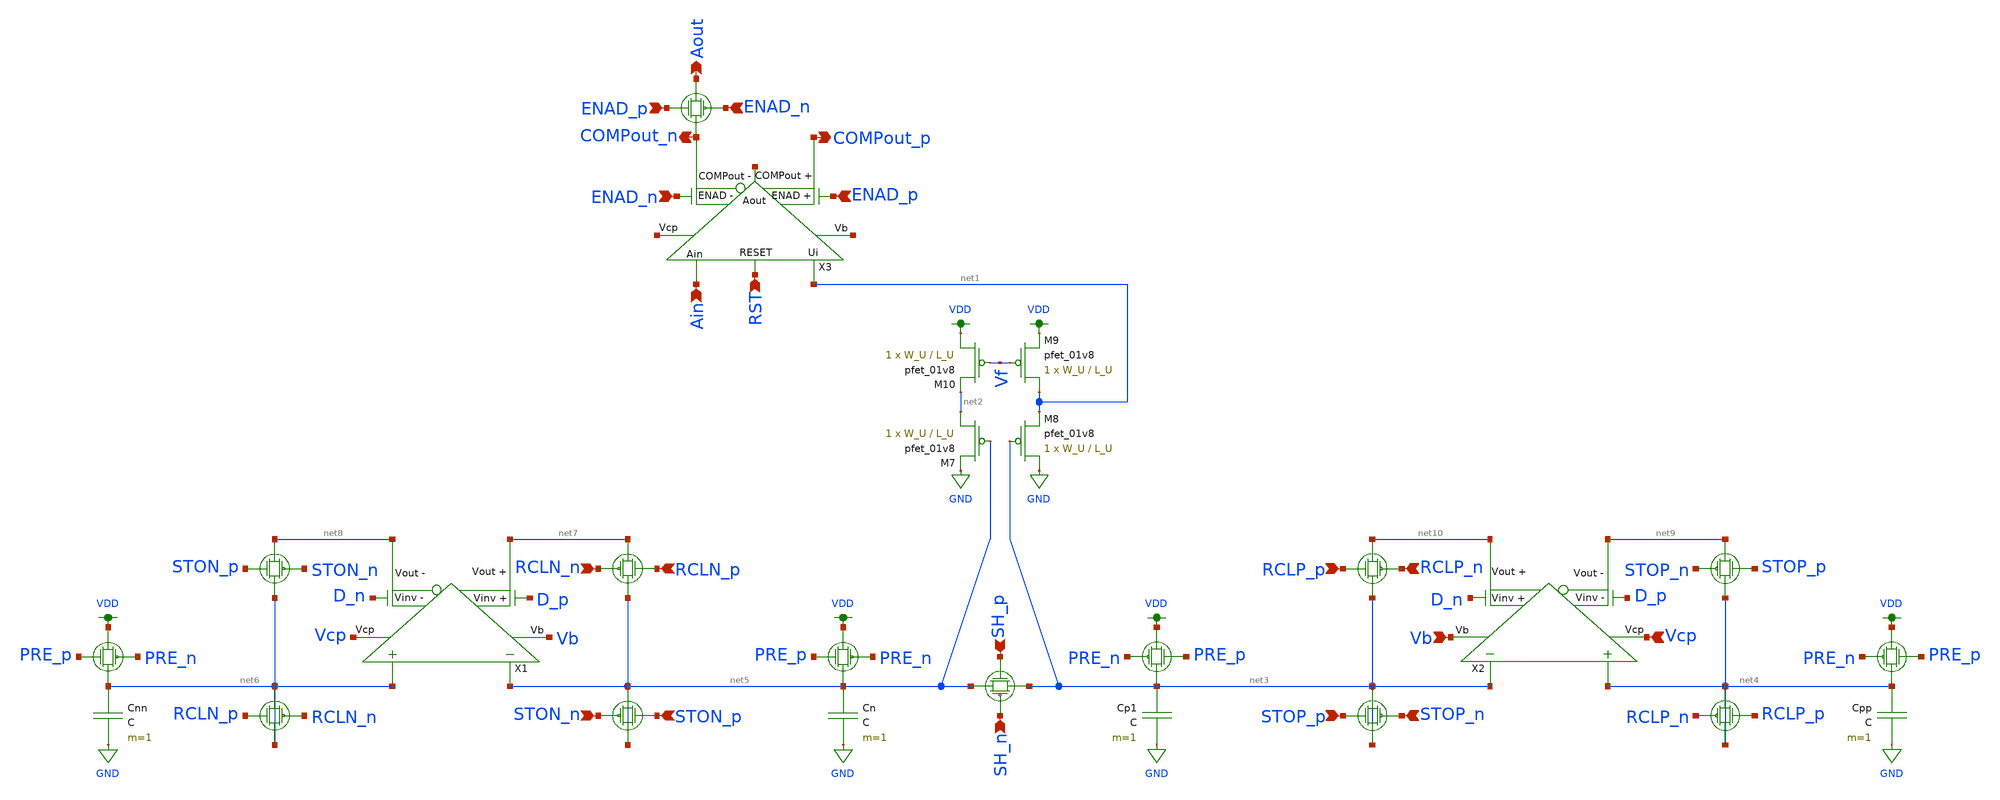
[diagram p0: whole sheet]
** sch_path: schematics/toplevel_pretty.sch
**.subckt toplevel_pretty RCLP_p STOP_p RCLP_n STOP_n SH_p SH_n Vb Vcp RCLN_p STON_p RCLN_n STON_n
*+ RST Ain Aout COMPout_n COMPout_p ENAD_p ENAD_n ENAD_p ENAD_n
*.ipin RCLP_p
*.ipin STOP_p
*.ipin RCLP_n
*.ipin STOP_n
*.ipin SH_p
*.ipin SH_n
*.ipin Vb
*.ipin Vcp
*.ipin RCLN_p
*.ipin STON_p
*.ipin RCLN_n
*.ipin STON_n
*.ipin RST
*.ipin Ain
*.opin Aout
*.opin COMPout_n
*.opin COMPout_p
*.ipin ENAD_p
*.ipin ENAD_n
*.ipin ENAD_p
*.ipin ENAD_n
X1 D_n net8 net7 Vcp Vb net5 net6 D_p ota
X2 D_p net9 net10 Vcp Vb net3 net4 D_n ota
X3 ENAD_n COMPout_n COMPout_p net11 net1 Ain ENAD_p net12 net13 RST comp_pretty
Cp1 net3 GND C m=1
XM7 net2 net5 GND VDD sky130_fd_pr__pfet_01v8 L=L_U W=W_U nf=1 ad='int((nf+1)/2) * W/nf * 0.29' as='int((nf+2)/2) * W/nf * 0.29'
+ pd='2*int((nf+1)/2) * (W/nf + 0.29)' ps='2*int((nf+2)/2) * (W/nf + 0.29)' nrd='0.29 / W' nrs='0.29 / W'
+ sa=0 sb=0 sd=0 mult=1 m=1
XM8 GND net3 net1 VDD sky130_fd_pr__pfet_01v8 L=L_U W=W_U nf=1 ad='int((nf+1)/2) * W/nf * 0.29' as='int((nf+2)/2) * W/nf * 0.29'
+ pd='2*int((nf+1)/2) * (W/nf + 0.29)' ps='2*int((nf+2)/2) * (W/nf + 0.29)' nrd='0.29 / W' nrs='0.29 / W'
+ sa=0 sb=0 sd=0 mult=1 m=1
XM9 net1 Vf VDD VDD sky130_fd_pr__pfet_01v8 L=L_U W=W_U nf=1 ad='int((nf+1)/2) * W/nf * 0.29' as='int((nf+2)/2) * W/nf * 0.29'
+ pd='2*int((nf+1)/2) * (W/nf + 0.29)' ps='2*int((nf+2)/2) * (W/nf + 0.29)' nrd='0.29 / W' nrs='0.29 / W'
+ sa=0 sb=0 sd=0 mult=1 m=1
XM10 VDD Vf net2 VDD sky130_fd_pr__pfet_01v8 L=L_U W=W_U nf=1 ad='int((nf+1)/2) * W/nf * 0.29' as='int((nf+2)/2) * W/nf * 0.29'
+ pd='2*int((nf+1)/2) * (W/nf + 0.29)' ps='2*int((nf+2)/2) * (W/nf + 0.29)' nrd='0.29 / W' nrs='0.29 / W'
+ sa=0 sb=0 sd=0 mult=1 m=1
Cpp net4 GND C m=1
Cn net5 GND C m=1
Cnn net6 GND C m=1
**.ends

* expanding   symbol:  ENGR3426-MADVLSI/final_project/schematics/ota.sym # of pins=8
** sym_path: schematics/ota.sym
** sch_path: schematics/ota.sch
.subckt ota Vinv_n Vout_n Vout_p Vcp Vb Vin_n Vin_p Vinv_p
*.ipin Vin_n
*.ipin Vin_p
*.opin Vout_n
*.opin Vout_p
*.ipin Vcp
*.ipin Vb
*.ipin Vinv_p
*.ipin Vinv_n
XM18 net3 net3 VDD VDD sky130_fd_pr__pfet_01v8 L=L_U W=W_U nf=1 ad='int((nf+1)/2) * W/nf * 0.29' as='int((nf+2)/2) * W/nf * 0.29'
+ pd='2*int((nf+1)/2) * (W/nf + 0.29)' ps='2*int((nf+2)/2) * (W/nf + 0.29)' nrd='0.29 / W' nrs='0.29 / W'
+ sa=0 sb=0 sd=0 mult=1 m=1
XM19 net4 Vin_n net1 GND sky130_fd_pr__nfet_01v8 L=L_U W=W_U nf=1 ad='int((nf+1)/2) * W/nf * 0.29' as='int((nf+2)/2) * W/nf * 0.29'
+ pd='2*int((nf+1)/2) * (W/nf + 0.29)' ps='2*int((nf+2)/2) * (W/nf + 0.29)' nrd='0.29 / W' nrs='0.29 / W'
+ sa=0 sb=0 sd=0 mult=1 m=1
XM20 net3 Vin_p net1 GND sky130_fd_pr__nfet_01v8 L=L_U W=W_U nf=1 ad='int((nf+1)/2) * W/nf * 0.29' as='int((nf+2)/2) * W/nf * 0.29'
+ pd='2*int((nf+1)/2) * (W/nf + 0.29)' ps='2*int((nf+2)/2) * (W/nf + 0.29)' nrd='0.29 / W' nrs='0.29 / W'
+ sa=0 sb=0 sd=0 mult=1 m=1
XM21 net1 Vb GND GND sky130_fd_pr__nfet_01v8 L=L_U W=W_U nf=1 ad='int((nf+1)/2) * W/nf * 0.29' as='int((nf+2)/2) * W/nf * 0.29'
+ pd='2*int((nf+1)/2) * (W/nf + 0.29)' ps='2*int((nf+2)/2) * (W/nf + 0.29)' nrd='0.29 / W' nrs='0.29 / W'
+ sa=0 sb=0 sd=0 mult=1 m=1
XM22 net4 net4 VDD VDD sky130_fd_pr__pfet_01v8 L=L_U W=W_U nf=1 ad='int((nf+1)/2) * W/nf * 0.29' as='int((nf+2)/2) * W/nf * 0.29'
+ pd='2*int((nf+1)/2) * (W/nf + 0.29)' ps='2*int((nf+2)/2) * (W/nf + 0.29)' nrd='0.29 / W' nrs='0.29 / W'
+ sa=0 sb=0 sd=0 mult=1 m=1
XM23 net8 net3 VDD VDD sky130_fd_pr__pfet_01v8 L=L_U W=W_U nf=1 ad='int((nf+1)/2) * W/nf * 0.29' as='int((nf+2)/2) * W/nf * 0.29'
+ pd='2*int((nf+1)/2) * (W/nf + 0.29)' ps='2*int((nf+2)/2) * (W/nf + 0.29)' nrd='0.29 / W' nrs='0.29 / W'
+ sa=0 sb=0 sd=0 mult=1 m=1
XM24 net9 net4 VDD VDD sky130_fd_pr__pfet_01v8 L=L_U W=W_U nf=1 ad='int((nf+1)/2) * W/nf * 0.29' as='int((nf+2)/2) * W/nf * 0.29'
+ pd='2*int((nf+1)/2) * (W/nf + 0.29)' ps='2*int((nf+2)/2) * (W/nf + 0.29)' nrd='0.29 / W' nrs='0.29 / W'
+ sa=0 sb=0 sd=0 mult=1 m=1
XM25 net9 Vcp Vout_n VDD sky130_fd_pr__pfet_01v8 L=L_U W=W_U nf=1 ad='int((nf+1)/2) * W/nf * 0.29' as='int((nf+2)/2) * W/nf * 0.29'
+ pd='2*int((nf+1)/2) * (W/nf + 0.29)' ps='2*int((nf+2)/2) * (W/nf + 0.29)' nrd='0.29 / W' nrs='0.29 / W'
+ sa=0 sb=0 sd=0 mult=1 m=1
XM26 Vout_p Vcp net8 VDD sky130_fd_pr__pfet_01v8 L=L_U W=W_U nf=1 ad='int((nf+1)/2) * W/nf * 0.29' as='int((nf+2)/2) * W/nf * 0.29'
+ pd='2*int((nf+1)/2) * (W/nf + 0.29)' ps='2*int((nf+2)/2) * (W/nf + 0.29)' nrd='0.29 / W' nrs='0.29 / W'
+ sa=0 sb=0 sd=0 mult=1 m=1
XM27 Vout_p net7 net5 GND sky130_fd_pr__nfet_01v8 L=L_U W=W_U nf=1 ad='int((nf+1)/2) * W/nf * 0.29' as='int((nf+2)/2) * W/nf * 0.29'
+ pd='2*int((nf+1)/2) * (W/nf + 0.29)' ps='2*int((nf+2)/2) * (W/nf + 0.29)' nrd='0.29 / W' nrs='0.29 / W'
+ sa=0 sb=0 sd=0 mult=1 m=1
XM28 Vout_n net7 net2 GND sky130_fd_pr__nfet_01v8 L=L_U W=W_U nf=1 ad='int((nf+1)/2) * W/nf * 0.29' as='int((nf+2)/2) * W/nf * 0.29'
+ pd='2*int((nf+1)/2) * (W/nf + 0.29)' ps='2*int((nf+2)/2) * (W/nf + 0.29)' nrd='0.29 / W' nrs='0.29 / W'
+ sa=0 sb=0 sd=0 mult=1 m=1
XM29 net5 net6 GND GND sky130_fd_pr__nfet_01v8 L=L_U W=W_U nf=1 ad='int((nf+1)/2) * W/nf * 0.29' as='int((nf+2)/2) * W/nf * 0.29'
+ pd='2*int((nf+1)/2) * (W/nf + 0.29)' ps='2*int((nf+2)/2) * (W/nf + 0.29)' nrd='0.29 / W' nrs='0.29 / W'
+ sa=0 sb=0 sd=0 mult=1 m=1
XM30 net5 Vinv_p net6 GND sky130_fd_pr__nfet_01v8 L=L_U W=W_U nf=1 ad='int((nf+1)/2) * W/nf * 0.29' as='int((nf+2)/2) * W/nf * 0.29'
+ pd='2*int((nf+1)/2) * (W/nf + 0.29)' ps='2*int((nf+2)/2) * (W/nf + 0.29)' nrd='0.29 / W' nrs='0.29 / W'
+ sa=0 sb=0 sd=0 mult=1 m=1
XM31 Vout_p Vinv_p net7 GND sky130_fd_pr__nfet_01v8 L=L_U W=W_U nf=1 ad='int((nf+1)/2) * W/nf * 0.29'
+ as='int((nf+2)/2) * W/nf * 0.29' pd='2*int((nf+1)/2) * (W/nf + 0.29)' ps='2*int((nf+2)/2) * (W/nf + 0.29)'
+ nrd='0.29 / W' nrs='0.29 / W' sa=0 sb=0 sd=0 mult=1 m=1
XM32 net2 net6 GND GND sky130_fd_pr__nfet_01v8 L=L_U W=W_U nf=1 ad='int((nf+1)/2) * W/nf * 0.29' as='int((nf+2)/2) * W/nf * 0.29'
+ pd='2*int((nf+1)/2) * (W/nf + 0.29)' ps='2*int((nf+2)/2) * (W/nf + 0.29)' nrd='0.29 / W' nrs='0.29 / W'
+ sa=0 sb=0 sd=0 mult=1 m=1
XM33 Vout_n Vinv_n net7 GND sky130_fd_pr__nfet_01v8 L=L_U W=W_U nf=1 ad='int((nf+1)/2) * W/nf * 0.29'
+ as='int((nf+2)/2) * W/nf * 0.29' pd='2*int((nf+1)/2) * (W/nf + 0.29)' ps='2*int((nf+2)/2) * (W/nf + 0.29)'
+ nrd='0.29 / W' nrs='0.29 / W' sa=0 sb=0 sd=0 mult=1 m=1
XM34 net2 Vinv_n net6 GND sky130_fd_pr__nfet_01v8 L=L_U W=W_U nf=1 ad='int((nf+1)/2) * W/nf * 0.29' as='int((nf+2)/2) * W/nf * 0.29'
+ pd='2*int((nf+1)/2) * (W/nf + 0.29)' ps='2*int((nf+2)/2) * (W/nf + 0.29)' nrd='0.29 / W' nrs='0.29 / W'
+ sa=0 sb=0 sd=0 mult=1 m=1
.ends


* expanding   symbol:  ENGR3426-MADVLSI/final_project/schematics/comp_pretty.sym # of pins=10
** sym_path: schematics/comp_pretty.sym
** sch_path: schematics/comp_pretty.sch
.subckt comp_pretty ENAD_n COMPout_n COMPout_p Vb Ui Ain ENAD_p Aout Vcp RST
*.ipin Ain
*.ipin Vcp
*.ipin Vb
*.opin Aout
*.opin COMPout_n
*.opin COMPout_p
*.ipin ENAD_n
*.ipin RST
*.ipin Ui
*.ipin ENAD_p
XM1 net1 net1 VDD VDD sky130_fd_pr__pfet_01v8 L=L_U W=W_U nf=1 ad='int((nf+1)/2) * W/nf * 0.29' as='int((nf+2)/2) * W/nf * 0.29'
+ pd='2*int((nf+1)/2) * (W/nf + 0.29)' ps='2*int((nf+2)/2) * (W/nf + 0.29)' nrd='0.29 / W' nrs='0.29 / W'
+ sa=0 sb=0 sd=0 mult=1 m=1
XM2 net2 Ain net5 GND sky130_fd_pr__nfet_01v8 L=L_U W=W_U nf=1 ad='int((nf+1)/2) * W/nf * 0.29' as='int((nf+2)/2) * W/nf * 0.29'
+ pd='2*int((nf+1)/2) * (W/nf + 0.29)' ps='2*int((nf+2)/2) * (W/nf + 0.29)' nrd='0.29 / W' nrs='0.29 / W'
+ sa=0 sb=0 sd=0 mult=1 m=1
XM3 net1 Ui net5 GND sky130_fd_pr__nfet_01v8 L=L_U W=W_U nf=1 ad='int((nf+1)/2) * W/nf * 0.29' as='int((nf+2)/2) * W/nf * 0.29'
+ pd='2*int((nf+1)/2) * (W/nf + 0.29)' ps='2*int((nf+2)/2) * (W/nf + 0.29)' nrd='0.29 / W' nrs='0.29 / W'
+ sa=0 sb=0 sd=0 mult=1 m=1
XM4 net5 Vb GND GND sky130_fd_pr__nfet_01v8 L=L_U W=W_U nf=1 ad='int((nf+1)/2) * W/nf * 0.29' as='int((nf+2)/2) * W/nf * 0.29'
+ pd='2*int((nf+1)/2) * (W/nf + 0.29)' ps='2*int((nf+2)/2) * (W/nf + 0.29)' nrd='0.29 / W' nrs='0.29 / W'
+ sa=0 sb=0 sd=0 mult=1 m=1
XM5 net2 net2 VDD VDD sky130_fd_pr__pfet_01v8 L=L_U W=W_U nf=1 ad='int((nf+1)/2) * W/nf * 0.29' as='int((nf+2)/2) * W/nf * 0.29'
+ pd='2*int((nf+1)/2) * (W/nf + 0.29)' ps='2*int((nf+2)/2) * (W/nf + 0.29)' nrd='0.29 / W' nrs='0.29 / W'
+ sa=0 sb=0 sd=0 mult=1 m=1
XM6 net8 net1 VDD VDD sky130_fd_pr__pfet_01v8 L=L_U W=W_U nf=1 ad='int((nf+1)/2) * W/nf * 0.29' as='int((nf+2)/2) * W/nf * 0.29'
+ pd='2*int((nf+1)/2) * (W/nf + 0.29)' ps='2*int((nf+2)/2) * (W/nf + 0.29)' nrd='0.29 / W' nrs='0.29 / W'
+ sa=0 sb=0 sd=0 mult=1 m=1
XM7 net9 net2 VDD VDD sky130_fd_pr__pfet_01v8 L=L_U W=W_U nf=1 ad='int((nf+1)/2) * W/nf * 0.29' as='int((nf+2)/2) * W/nf * 0.29'
+ pd='2*int((nf+1)/2) * (W/nf + 0.29)' ps='2*int((nf+2)/2) * (W/nf + 0.29)' nrd='0.29 / W' nrs='0.29 / W'
+ sa=0 sb=0 sd=0 mult=1 m=1
XM8 net9 Vcp COMPout_p VDD sky130_fd_pr__pfet_01v8 L=L_U W=W_U nf=1 ad='int((nf+1)/2) * W/nf * 0.29'
+ as='int((nf+2)/2) * W/nf * 0.29' pd='2*int((nf+1)/2) * (W/nf + 0.29)' ps='2*int((nf+2)/2) * (W/nf + 0.29)'
+ nrd='0.29 / W' nrs='0.29 / W' sa=0 sb=0 sd=0 mult=1 m=1
XM9 COMPout_n Vcp net8 VDD sky130_fd_pr__pfet_01v8 L=L_U W=W_U nf=1 ad='int((nf+1)/2) * W/nf * 0.29'
+ as='int((nf+2)/2) * W/nf * 0.29' pd='2*int((nf+1)/2) * (W/nf + 0.29)' ps='2*int((nf+2)/2) * (W/nf + 0.29)'
+ nrd='0.29 / W' nrs='0.29 / W' sa=0 sb=0 sd=0 mult=1 m=1
XM10 net1 Vb GND GND sky130_fd_pr__nfet_01v8 L=L_U W=W_U nf=1 ad='int((nf+1)/2) * W/nf * 0.29' as='int((nf+2)/2) * W/nf * 0.29'
+ pd='2*int((nf+1)/2) * (W/nf + 0.29)' ps='2*int((nf+2)/2) * (W/nf + 0.29)' nrd='0.29 / W' nrs='0.29 / W'
+ sa=0 sb=0 sd=0 mult=1 m=1
XM11 net2 Vb GND GND sky130_fd_pr__nfet_01v8 L=L_U W=W_U nf=1 ad='int((nf+1)/2) * W/nf * 0.29' as='int((nf+2)/2) * W/nf * 0.29'
+ pd='2*int((nf+1)/2) * (W/nf + 0.29)' ps='2*int((nf+2)/2) * (W/nf + 0.29)' nrd='0.29 / W' nrs='0.29 / W'
+ sa=0 sb=0 sd=0 mult=1 m=1
XM12 COMPout_n net6 net4 GND sky130_fd_pr__nfet_01v8 L=L_U W=W_U nf=1 ad='int((nf+1)/2) * W/nf * 0.29'
+ as='int((nf+2)/2) * W/nf * 0.29' pd='2*int((nf+1)/2) * (W/nf + 0.29)' ps='2*int((nf+2)/2) * (W/nf + 0.29)'
+ nrd='0.29 / W' nrs='0.29 / W' sa=0 sb=0 sd=0 mult=1 m=1
XM13 net6 ENAD_n VDD VDD sky130_fd_pr__pfet_01v8 L=L_U W=W_U nf=1 ad='int((nf+1)/2) * W/nf * 0.29' as='int((nf+2)/2) * W/nf * 0.29'
+ pd='2*int((nf+1)/2) * (W/nf + 0.29)' ps='2*int((nf+2)/2) * (W/nf + 0.29)' nrd='0.29 / W' nrs='0.29 / W'
+ sa=0 sb=0 sd=0 mult=1 m=1
XM14 COMPout_p net6 net3 GND sky130_fd_pr__nfet_01v8 L=L_U W=W_U nf=1 ad='int((nf+1)/2) * W/nf * 0.29'
+ as='int((nf+2)/2) * W/nf * 0.29' pd='2*int((nf+1)/2) * (W/nf + 0.29)' ps='2*int((nf+2)/2) * (W/nf + 0.29)'
+ nrd='0.29 / W' nrs='0.29 / W' sa=0 sb=0 sd=0 mult=1 m=1
XM15 COMPout_p ENAD_n net6 GND sky130_fd_pr__nfet_01v8 L=L_U W=W_U nf=1 ad='int((nf+1)/2) * W/nf * 0.29'
+ as='int((nf+2)/2) * W/nf * 0.29' pd='2*int((nf+1)/2) * (W/nf + 0.29)' ps='2*int((nf+2)/2) * (W/nf + 0.29)'
+ nrd='0.29 / W' nrs='0.29 / W' sa=0 sb=0 sd=0 mult=1 m=1
XM16 net4 net3 GND GND sky130_fd_pr__nfet_01v8 L=L_U W=W_U nf=1 ad='int((nf+1)/2) * W/nf * 0.29' as='int((nf+2)/2) * W/nf * 0.29'
+ pd='2*int((nf+1)/2) * (W/nf + 0.29)' ps='2*int((nf+2)/2) * (W/nf + 0.29)' nrd='0.29 / W' nrs='0.29 / W'
+ sa=0 sb=0 sd=0 mult=1 m=1
XM17 net3 net7 GND GND sky130_fd_pr__nfet_01v8 L=L_U W=W_U nf=1 ad='int((nf+1)/2) * W/nf * 0.29' as='int((nf+2)/2) * W/nf * 0.29'
+ pd='2*int((nf+1)/2) * (W/nf + 0.29)' ps='2*int((nf+2)/2) * (W/nf + 0.29)' nrd='0.29 / W' nrs='0.29 / W'
+ sa=0 sb=0 sd=0 mult=1 m=1
XM18 net7 ENAD_n net3 GND sky130_fd_pr__nfet_01v8 L=L_U W=W_U nf=1 ad='int((nf+1)/2) * W/nf * 0.29' as='int((nf+2)/2) * W/nf * 0.29'
+ pd='2*int((nf+1)/2) * (W/nf + 0.29)' ps='2*int((nf+2)/2) * (W/nf + 0.29)' nrd='0.29 / W' nrs='0.29 / W'
+ sa=0 sb=0 sd=0 mult=1 m=1
XM19 net4 ENAD_p net7 GND sky130_fd_pr__nfet_01v8 L=L_U W=W_U nf=1 ad='int((nf+1)/2) * W/nf * 0.29' as='int((nf+2)/2) * W/nf * 0.29'
+ pd='2*int((nf+1)/2) * (W/nf + 0.29)' ps='2*int((nf+2)/2) * (W/nf + 0.29)' nrd='0.29 / W' nrs='0.29 / W'
+ sa=0 sb=0 sd=0 mult=1 m=1
XM20 net7 RST net3 GND sky130_fd_pr__nfet_01v8 L=L_U W=W_U nf=1 ad='int((nf+1)/2) * W/nf * 0.29' as='int((nf+2)/2) * W/nf * 0.29'
+ pd='2*int((nf+1)/2) * (W/nf + 0.29)' ps='2*int((nf+2)/2) * (W/nf + 0.29)' nrd='0.29 / W' nrs='0.29 / W'
+ sa=0 sb=0 sd=0 mult=1 m=1
C1 net3 GND 1p m=1
C2 net7 GND 1p m=1
XM26 COMPout_n ENAD_n Aout VDD sky130_fd_pr__pfet_01v8 L=L_U W=W_U nf=1 ad='int((nf+1)/2) * W/nf * 0.29'
+ as='int((nf+2)/2) * W/nf * 0.29' pd='2*int((nf+1)/2) * (W/nf + 0.29)' ps='2*int((nf+2)/2) * (W/nf + 0.29)'
+ nrd='0.29 / W' nrs='0.29 / W' sa=0 sb=0 sd=0 mult=1 m=1
XM27 Aout ENAD_p COMPout_n GND sky130_fd_pr__nfet_01v8 L=L_U W=W_U nf=1 ad='int((nf+1)/2) * W/nf * 0.29'
+ as='int((nf+2)/2) * W/nf * 0.29' pd='2*int((nf+1)/2) * (W/nf + 0.29)' ps='2*int((nf+2)/2) * (W/nf + 0.29)'
+ nrd='0.29 / W' nrs='0.29 / W' sa=0 sb=0 sd=0 mult=1 m=1
.ends

.GLOBAL GND
.GLOBAL VDD
.end
